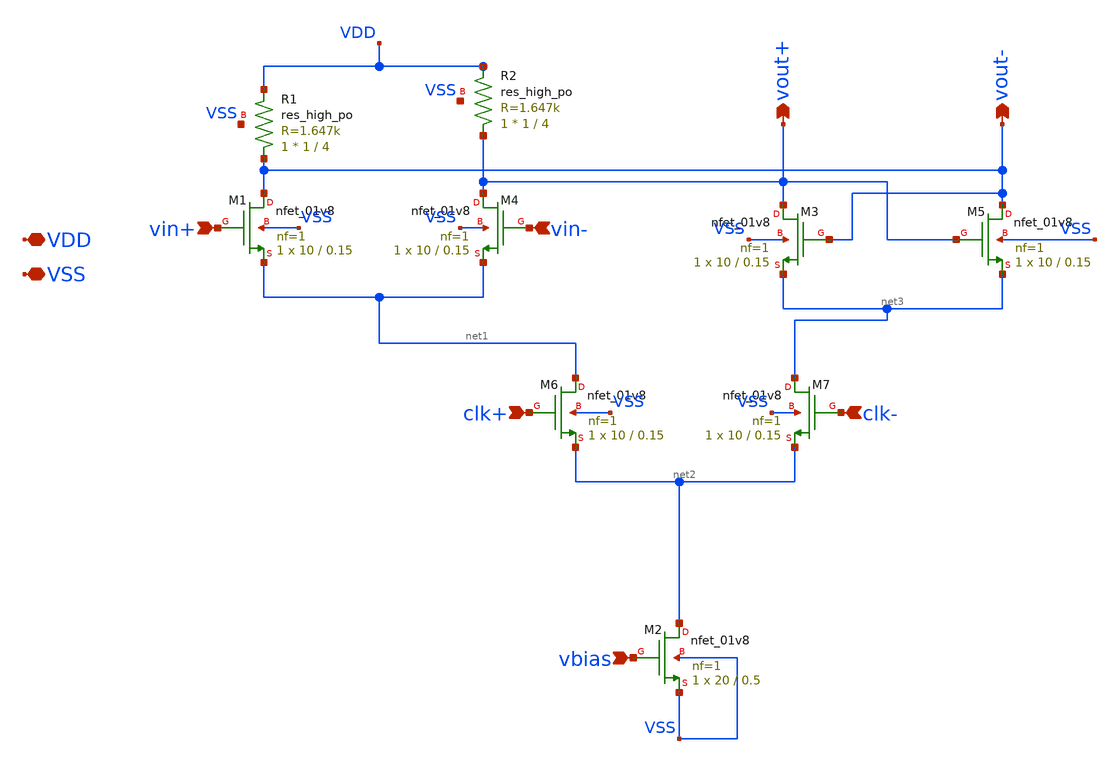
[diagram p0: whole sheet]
** sch_path: xschem/d_latch.sch
**.subckt d_latch VDD VSS vin+ clk- vbias vout+ clk+ vout- vin-
*.iopin VDD
*.iopin VSS
*.ipin vin+
*.ipin clk-
*.ipin vbias
*.opin vout+
*.ipin clk+
*.opin vout-
*.ipin vin-
XM1 vout- vin+ net1 VSS sky130_fd_pr__nfet_01v8 L=0.15 W=10 nf=1 ad='int((nf+1)/2) * W/nf * 0.29' as='int((nf+2)/2) * W/nf * 0.29'
+ pd='2*int((nf+1)/2) * (W/nf + 0.29)' ps='2*int((nf+2)/2) * (W/nf + 0.29)' nrd='0.29 / W' nrs='0.29 / W'
+ sa=0 sb=0 sd=0 mult=1 m=1
XM2 net2 vbias VSS VSS sky130_fd_pr__nfet_01v8 L=0.5 W=20 nf=1 ad='int((nf+1)/2) * W/nf * 0.29' as='int((nf+2)/2) * W/nf * 0.29'
+ pd='2*int((nf+1)/2) * (W/nf + 0.29)' ps='2*int((nf+2)/2) * (W/nf + 0.29)' nrd='0.29 / W' nrs='0.29 / W'
+ sa=0 sb=0 sd=0 mult=1 m=1
XM4 vout+ vin- net1 VSS sky130_fd_pr__nfet_01v8 L=0.15 W=10 nf=1 ad='int((nf+1)/2) * W/nf * 0.29' as='int((nf+2)/2) * W/nf * 0.29'
+ pd='2*int((nf+1)/2) * (W/nf + 0.29)' ps='2*int((nf+2)/2) * (W/nf + 0.29)' nrd='0.29 / W' nrs='0.29 / W'
+ sa=0 sb=0 sd=0 mult=1 m=1
XR1 vout- VDD VSS sky130_fd_pr__res_high_po W=1 L=4 mult=1 m=1
XR2 vout+ VDD VSS sky130_fd_pr__res_high_po W=1 L=4 mult=1 m=1
XM3 vout+ vout- net3 VSS sky130_fd_pr__nfet_01v8 L=0.15 W=10 nf=1 ad='int((nf+1)/2) * W/nf * 0.29' as='int((nf+2)/2) * W/nf * 0.29'
+ pd='2*int((nf+1)/2) * (W/nf + 0.29)' ps='2*int((nf+2)/2) * (W/nf + 0.29)' nrd='0.29 / W' nrs='0.29 / W'
+ sa=0 sb=0 sd=0 mult=1 m=1
XM5 vout- vout+ net3 VSS sky130_fd_pr__nfet_01v8 L=0.15 W=10 nf=1 ad='int((nf+1)/2) * W/nf * 0.29' as='int((nf+2)/2) * W/nf * 0.29'
+ pd='2*int((nf+1)/2) * (W/nf + 0.29)' ps='2*int((nf+2)/2) * (W/nf + 0.29)' nrd='0.29 / W' nrs='0.29 / W'
+ sa=0 sb=0 sd=0 mult=1 m=1
XM6 net1 clk+ net2 VSS sky130_fd_pr__nfet_01v8 L=0.15 W=10 nf=1 ad='int((nf+1)/2) * W/nf * 0.29' as='int((nf+2)/2) * W/nf * 0.29'
+ pd='2*int((nf+1)/2) * (W/nf + 0.29)' ps='2*int((nf+2)/2) * (W/nf + 0.29)' nrd='0.29 / W' nrs='0.29 / W'
+ sa=0 sb=0 sd=0 mult=1 m=1
XM7 net3 clk- net2 VSS sky130_fd_pr__nfet_01v8 L=0.15 W=10 nf=1 ad='int((nf+1)/2) * W/nf * 0.29' as='int((nf+2)/2) * W/nf * 0.29'
+ pd='2*int((nf+1)/2) * (W/nf + 0.29)' ps='2*int((nf+2)/2) * (W/nf + 0.29)' nrd='0.29 / W' nrs='0.29 / W'
+ sa=0 sb=0 sd=0 mult=1 m=1
**.ends
.end
